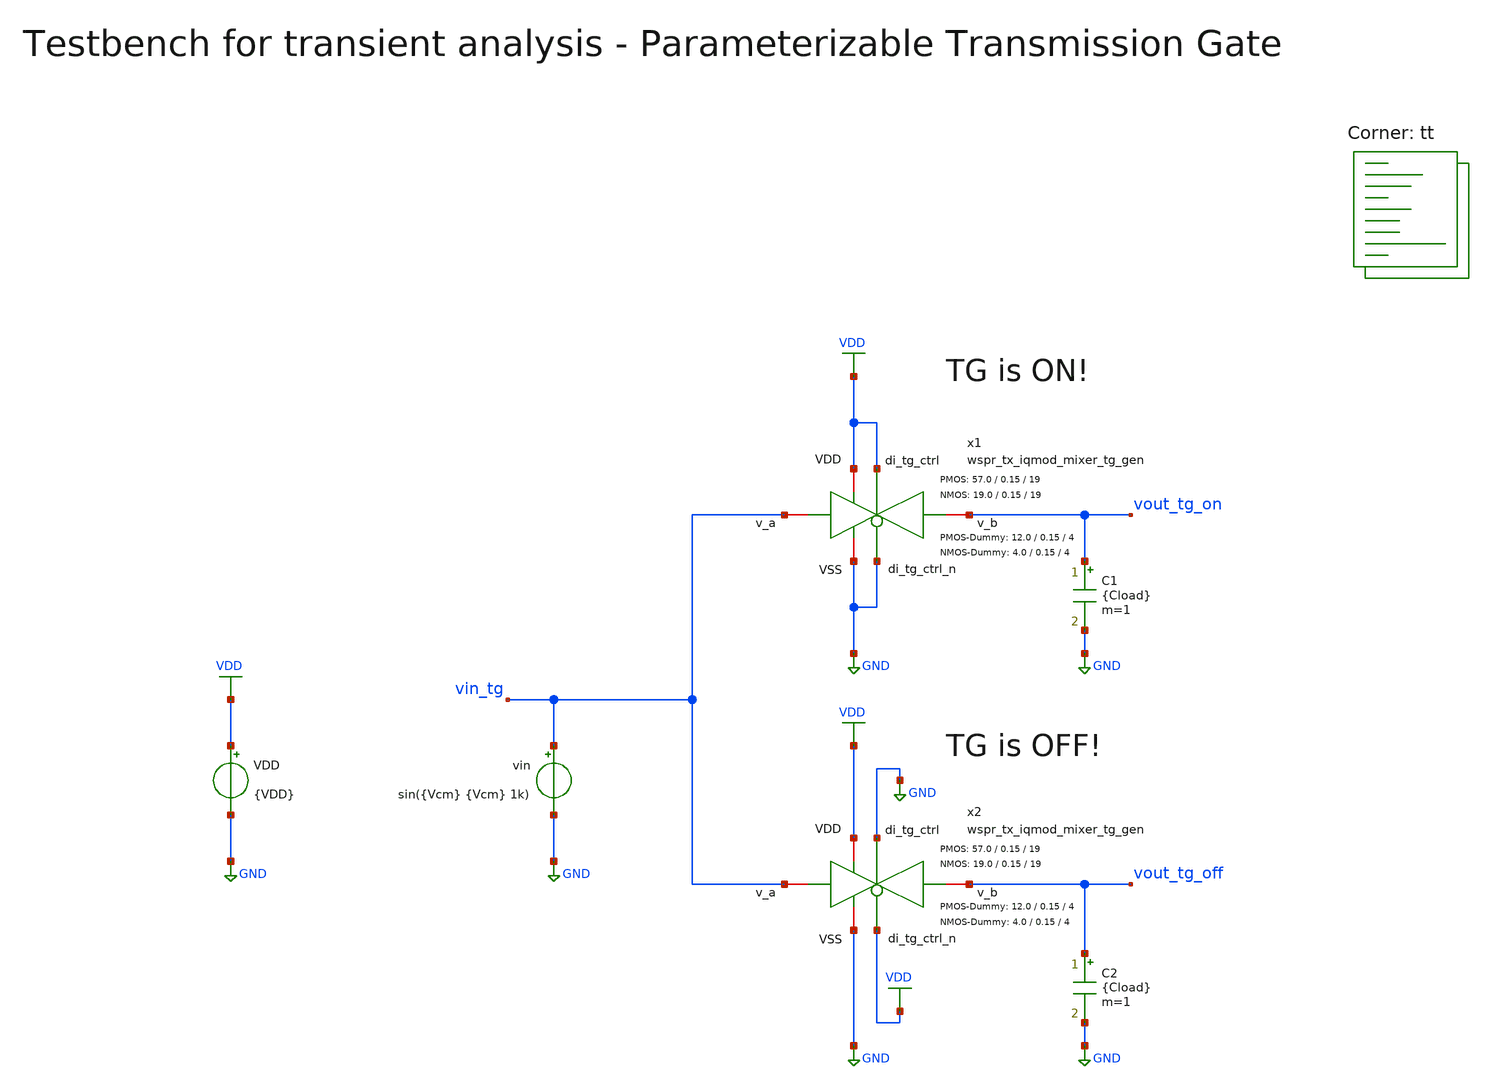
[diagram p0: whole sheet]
** sch_path: sky130/macros/iqmod/testbenches/wspr_tx_iqmod_mixer_tg_tb_tran.sch
**.subckt wspr_tx_iqmod_mixer_tg_tb_tran
VDD VDD GND {VDD}
vin vin_tg GND sin({Vcm} {Vcm} 1k)
C1 vout_tg_on GND {Cload} m=1
C2 vout_tg_off GND {Cload} m=1
x1 VDD VDD GND vout_tg_on vin_tg GND wspr_tx_iqmod_mixer_tg_gen W_P=57.0 L_P=0.15 NF_P=19 W_N=19.0
+ L_N=0.15 NF_N=19 W_P_D=12.0 L_P_D=0.15 NF_P_D=4 W_N_D=4.0 L_N_D=0.15 NF_N_D=4
x2 VDD GND GND vout_tg_off vin_tg VDD wspr_tx_iqmod_mixer_tg_gen W_P=57.0 L_P=0.15 NF_P=19 W_N=19.0
+ L_N=0.15 NF_N=19 W_P_D=12.0 L_P_D=0.15 NF_P_D=4 W_N_D=4.0 L_N_D=0.15 NF_N_D=4
**** begin user architecture code


.param VDD=1.8
.param Vcm=VDD/2
.param temp=27
.param Cload=10p
.param W_P=54
.param L_P=0.15
.param NF_P=6
.param W_N=18
.param L_N=0.15
.param NF_N=6
.param W_P_D=12.0
.param L_P_D=0.15
.param NF_P_D=4
.param W_N_D=4.0
.param L_N_D=0.15
.param NF_N_D=4
.options savecurrents klu method=gear reltol=1e-4 abstol=1e-15 gmin=1e-15
.control

save all

* Operating Point Analysis
op
remzerovec
write wspr_tx_iqmod_mixer_tg_tb_tran.raw
set appendwrite

* Transient Analysis
tran 10u 10ms
write wspr_tx_iqmod_mixer_tg_tb_tran.raw

plot vin_tg vout_tg_on
plot vin_tg vout_tg_off

* Writing Data
unset appendwrite
set wr_singlescale
set wr_vecnames
wrdata $PROJECT_PATH/python/plot_simulations/data/wspr_tx_iqmod_mixer_tg_tb_tran.txt v(vin_tg)
+ v(vout_tg_on) v(vout_tg_off)


*quit
.endc

.lib $::SKYWATER_MODELS/sky130.lib.spice tt
**** end user architecture code
**.ends
.GLOBAL GND
.GLOBAL VDD
.end
